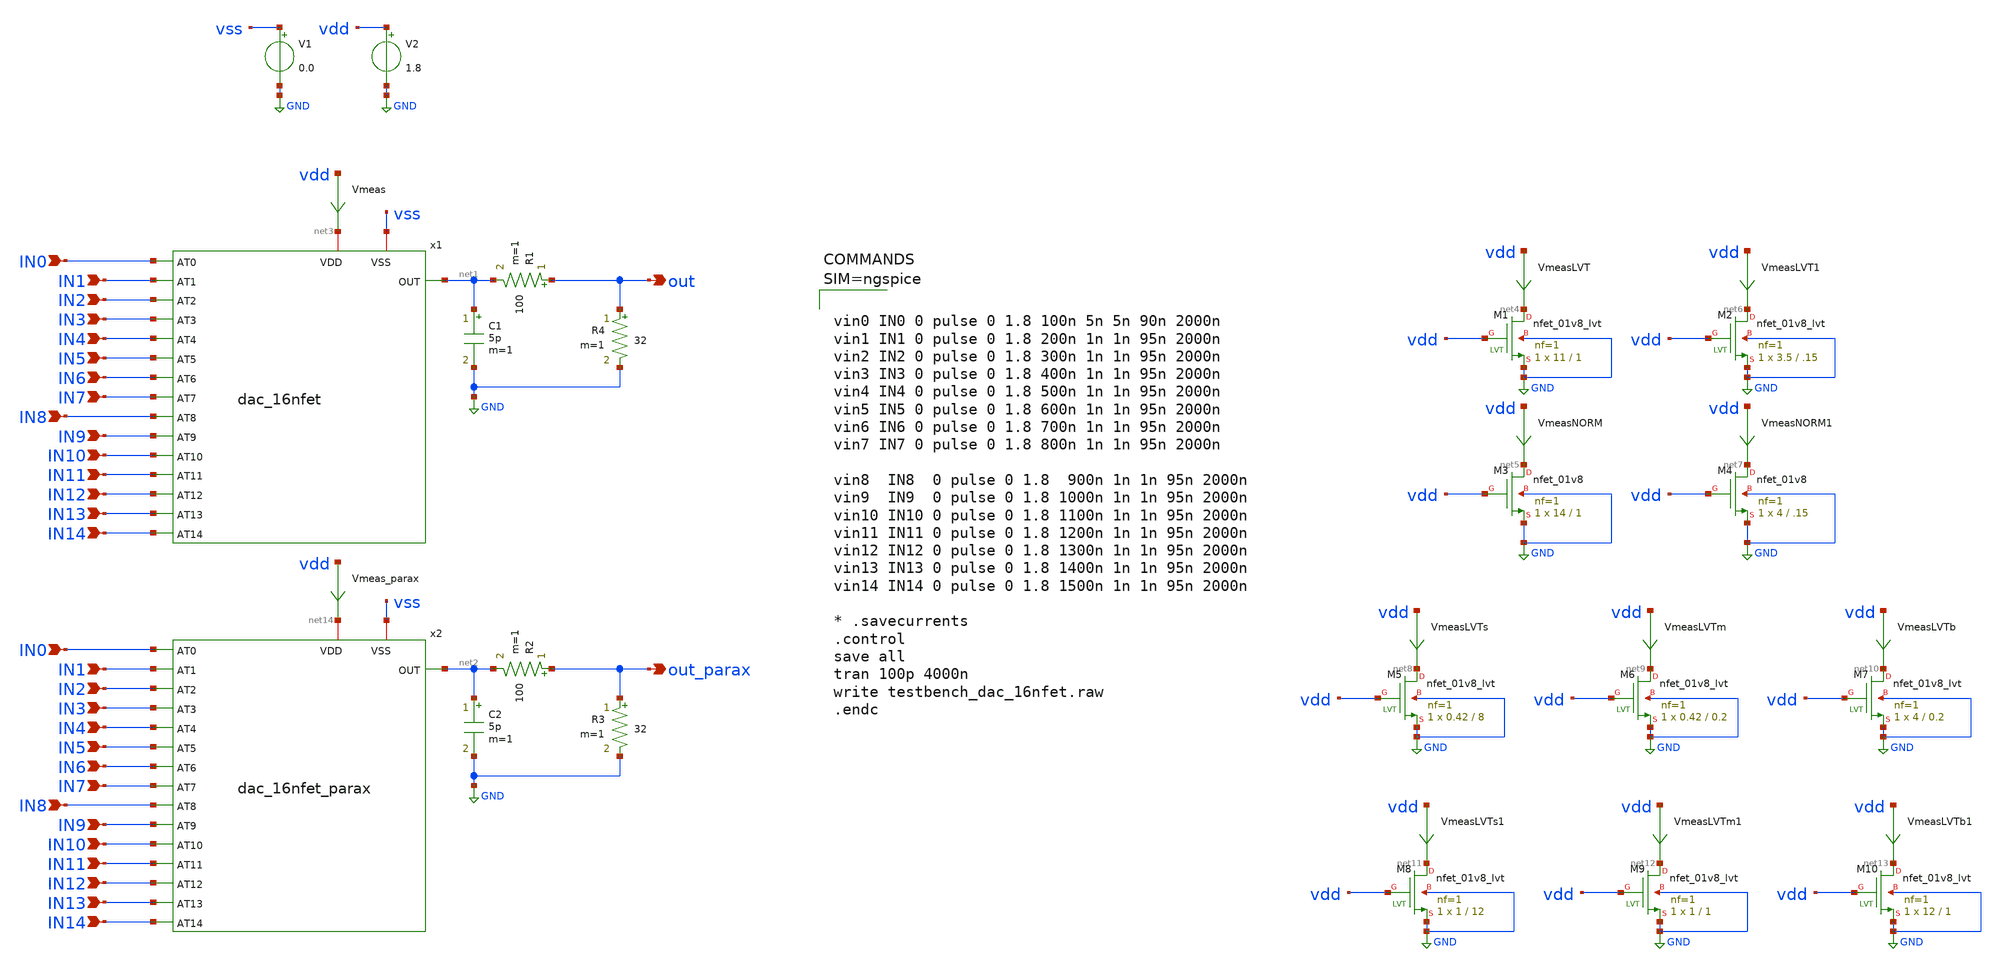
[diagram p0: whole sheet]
** sch_path: xschem/testbench_dac_16nfet.sch
**.subckt testbench_dac_16nfet IN1 out IN2 IN3 IN0 IN5 IN6 IN7 IN4 IN9 IN10 IN11 IN8 IN13 IN14 IN12
*+ IN1 out_parax IN2 IN3 IN0 IN5 IN6 IN7 IN4 IN9 IN10 IN11 IN8 IN13 IN14 IN12
*.ipin IN1
*.opin out
*.ipin IN2
*.ipin IN3
*.ipin IN0
*.ipin IN5
*.ipin IN6
*.ipin IN7
*.ipin IN4
*.ipin IN9
*.ipin IN10
*.ipin IN11
*.ipin IN8
*.ipin IN13
*.ipin IN14
*.ipin IN12
*.ipin IN1
*.opin out_parax
*.ipin IN2
*.ipin IN3
*.ipin IN0
*.ipin IN5
*.ipin IN6
*.ipin IN7
*.ipin IN4
*.ipin IN9
*.ipin IN10
*.ipin IN11
*.ipin IN8
*.ipin IN13
*.ipin IN14
*.ipin IN12
x1 net3 IN0 IN1 IN2 IN3 IN4 IN5 IN6 IN7 IN8 IN9 IN10 IN11 IN12 IN13 IN14 net1 vss dac_16nfet
V1 vss GND 0.0
V2 vdd GND 1.8
R1 out net1 100 m=1
Vmeas vdd net3 0
.save i(vmeas)
R4 out GND 32 m=1
C1 net1 GND 5p m=1
XM1 net4 vdd GND GND sky130_fd_pr__nfet_01v8_lvt L=1 W=11 nf=1 ad='int((nf+1)/2) * W/nf * 0.29' as='int((nf+2)/2) * W/nf * 0.29'
+ pd='2*int((nf+1)/2) * (W/nf + 0.29)' ps='2*int((nf+2)/2) * (W/nf + 0.29)' nrd='0.29 / W' nrs='0.29 / W'
+ sa=0 sb=0 sd=0 mult=1 m=1
VmeasLVT vdd net4 0
.save i(vmeaslvt)
XM3 net5 vdd GND GND sky130_fd_pr__nfet_01v8 L=1 W=14 nf=1 ad='int((nf+1)/2) * W/nf * 0.29' as='int((nf+2)/2) * W/nf * 0.29'
+ pd='2*int((nf+1)/2) * (W/nf + 0.29)' ps='2*int((nf+2)/2) * (W/nf + 0.29)' nrd='0.29 / W' nrs='0.29 / W'
+ sa=0 sb=0 sd=0 mult=1 m=1
VmeasNORM vdd net5 0
.save i(vmeasnorm)
XM2 net6 vdd GND GND sky130_fd_pr__nfet_01v8_lvt L=.15 W=3.5 nf=1 ad='int((nf+1)/2) * W/nf * 0.29' as='int((nf+2)/2) * W/nf * 0.29'
+ pd='2*int((nf+1)/2) * (W/nf + 0.29)' ps='2*int((nf+2)/2) * (W/nf + 0.29)' nrd='0.29 / W' nrs='0.29 / W'
+ sa=0 sb=0 sd=0 mult=1 m=1
VmeasLVT1 vdd net6 0
.save i(vmeaslvt1)
XM4 net7 vdd GND GND sky130_fd_pr__nfet_01v8 L=.15 W=4 nf=1 ad='int((nf+1)/2) * W/nf * 0.29' as='int((nf+2)/2) * W/nf * 0.29'
+ pd='2*int((nf+1)/2) * (W/nf + 0.29)' ps='2*int((nf+2)/2) * (W/nf + 0.29)' nrd='0.29 / W' nrs='0.29 / W'
+ sa=0 sb=0 sd=0 mult=1 m=1
VmeasNORM1 vdd net7 0
.save i(vmeasnorm1)
XM5 net8 vdd GND GND sky130_fd_pr__nfet_01v8_lvt L=8 W=0.42 nf=1 ad='int((nf+1)/2) * W/nf * 0.29' as='int((nf+2)/2) * W/nf * 0.29'
+ pd='2*int((nf+1)/2) * (W/nf + 0.29)' ps='2*int((nf+2)/2) * (W/nf + 0.29)' nrd='0.29 / W' nrs='0.29 / W'
+ sa=0 sb=0 sd=0 mult=1 m=1
VmeasLVTs vdd net8 0
.save i(vmeaslvts)
XM6 net9 vdd GND GND sky130_fd_pr__nfet_01v8_lvt L=0.2 W=0.42 nf=1 ad='int((nf+1)/2) * W/nf * 0.29' as='int((nf+2)/2) * W/nf * 0.29'
+ pd='2*int((nf+1)/2) * (W/nf + 0.29)' ps='2*int((nf+2)/2) * (W/nf + 0.29)' nrd='0.29 / W' nrs='0.29 / W'
+ sa=0 sb=0 sd=0 mult=1 m=1
VmeasLVTm vdd net9 0
.save i(vmeaslvtm)
XM7 net10 vdd GND GND sky130_fd_pr__nfet_01v8_lvt L=0.2 W=4 nf=1 ad='int((nf+1)/2) * W/nf * 0.29' as='int((nf+2)/2) * W/nf * 0.29'
+ pd='2*int((nf+1)/2) * (W/nf + 0.29)' ps='2*int((nf+2)/2) * (W/nf + 0.29)' nrd='0.29 / W' nrs='0.29 / W'
+ sa=0 sb=0 sd=0 mult=1 m=1
VmeasLVTb vdd net10 0
.save i(vmeaslvtb)
XM8 net11 vdd GND GND sky130_fd_pr__nfet_01v8_lvt L=12 W=1 nf=1 ad='int((nf+1)/2) * W/nf * 0.29' as='int((nf+2)/2) * W/nf * 0.29'
+ pd='2*int((nf+1)/2) * (W/nf + 0.29)' ps='2*int((nf+2)/2) * (W/nf + 0.29)' nrd='0.29 / W' nrs='0.29 / W'
+ sa=0 sb=0 sd=0 mult=1 m=1
VmeasLVTs1 vdd net11 0
.save i(vmeaslvts1)
XM9 net12 vdd GND GND sky130_fd_pr__nfet_01v8_lvt L=1 W=1 nf=1 ad='int((nf+1)/2) * W/nf * 0.29' as='int((nf+2)/2) * W/nf * 0.29'
+ pd='2*int((nf+1)/2) * (W/nf + 0.29)' ps='2*int((nf+2)/2) * (W/nf + 0.29)' nrd='0.29 / W' nrs='0.29 / W'
+ sa=0 sb=0 sd=0 mult=1 m=1
VmeasLVTm1 vdd net12 0
.save i(vmeaslvtm1)
XM10 net13 vdd GND GND sky130_fd_pr__nfet_01v8_lvt L=1 W=12 nf=1 ad='int((nf+1)/2) * W/nf * 0.29' as='int((nf+2)/2) * W/nf * 0.29'
+ pd='2*int((nf+1)/2) * (W/nf + 0.29)' ps='2*int((nf+2)/2) * (W/nf + 0.29)' nrd='0.29 / W' nrs='0.29 / W'
+ sa=0 sb=0 sd=0 mult=1 m=1
VmeasLVTb1 vdd net13 0
.save i(vmeaslvtb1)
x2 net14 IN0 IN1 IN2 IN3 IN4 IN5 IN6 IN7 IN8 IN9 IN10 IN11 IN12 IN13 IN14 net2 vss dac_16nfet_parax
R2 out_parax net2 100 m=1
Vmeas_parax vdd net14 0
.save i(vmeas_parax)
R3 out_parax GND 32 m=1
C2 net2 GND 5p m=1
**** begin user architecture code

** opencircuitdesign pdks install
.lib $::SKYWATER_MODELS/sky130.lib.spice tt





vin0 IN0 0 pulse 0 1.8 100n 5n 5n 90n 2000n
vin1 IN1 0 pulse 0 1.8 200n 1n 1n 95n 2000n
vin2 IN2 0 pulse 0 1.8 300n 1n 1n 95n 2000n
vin3 IN3 0 pulse 0 1.8 400n 1n 1n 95n 2000n
vin4 IN4 0 pulse 0 1.8 500n 1n 1n 95n 2000n
vin5 IN5 0 pulse 0 1.8 600n 1n 1n 95n 2000n
vin6 IN6 0 pulse 0 1.8 700n 1n 1n 95n 2000n
vin7 IN7 0 pulse 0 1.8 800n 1n 1n 95n 2000n

vin8  IN8  0 pulse 0 1.8  900n 1n 1n 95n 2000n
vin9  IN9  0 pulse 0 1.8 1000n 1n 1n 95n 2000n
vin10 IN10 0 pulse 0 1.8 1100n 1n 1n 95n 2000n
vin11 IN11 0 pulse 0 1.8 1200n 1n 1n 95n 2000n
vin12 IN12 0 pulse 0 1.8 1300n 1n 1n 95n 2000n
vin13 IN13 0 pulse 0 1.8 1400n 1n 1n 95n 2000n
vin14 IN14 0 pulse 0 1.8 1500n 1n 1n 95n 2000n

* .savecurrents
.control
save all
tran 100p 4000n
write testbench_dac_16nfet.raw
.endc



**** end user architecture code
**.ends

* expanding   symbol:  dac_16nfet.sym # of pins=18
** sym_path: xschem/dac_16nfet.sym
** sch_path: xschem/dac_16nfet.sch
.subckt dac_16nfet VDD AT0 AT1 AT2 AT3 AT4 AT5 AT6 AT7 AT8 AT9 AT10 AT11 AT12 AT13 AT14 OUT VSS
*.ipin AT12
*.ipin AT13
*.iopin VDD
*.iopin VSS
*.opin OUT
*.ipin AT14
*.ipin AT4
*.ipin AT5
*.ipin AT6
*.ipin AT7
*.ipin AT8
*.ipin AT9
*.ipin AT10
*.ipin AT11
*.ipin AT0
*.ipin AT1
*.ipin AT2
*.ipin AT3
XM1 VDD AT12 OUT VSS sky130_fd_pr__nfet_01v8 L=5.547 W=0.42 nf=1 ad='int((nf+1)/2) * W/nf * 0.29' as='int((nf+2)/2) * W/nf * 0.29'
+ pd='2*int((nf+1)/2) * (W/nf + 0.29)' ps='2*int((nf+2)/2) * (W/nf + 0.29)' nrd='0.29 / W' nrs='0.29 / W'
+ sa=0 sb=0 sd=0 mult=1 m=1
XM2 VDD AT13 OUT VSS sky130_fd_pr__nfet_01v8 L=7.784 W=0.42 nf=1 ad='int((nf+1)/2) * W/nf * 0.29' as='int((nf+2)/2) * W/nf * 0.29'
+ pd='2*int((nf+1)/2) * (W/nf + 0.29)' ps='2*int((nf+2)/2) * (W/nf + 0.29)' nrd='0.29 / W' nrs='0.29 / W'
+ sa=0 sb=0 sd=0 mult=1 m=1
XM3 VDD AT14 OUT VSS sky130_fd_pr__nfet_01v8 L=11.1 W=0.42 nf=1 ad='int((nf+1)/2) * W/nf * 0.29' as='int((nf+2)/2) * W/nf * 0.29'
+ pd='2*int((nf+1)/2) * (W/nf + 0.29)' ps='2*int((nf+2)/2) * (W/nf + 0.29)' nrd='0.29 / W' nrs='0.29 / W'
+ sa=0 sb=0 sd=0 mult=1 m=1
XM5 VDD AT8 OUT VSS sky130_fd_pr__nfet_01v8 L=1.386 W=0.42 nf=1 ad='int((nf+1)/2) * W/nf * 0.29' as='int((nf+2)/2) * W/nf * 0.29'
+ pd='2*int((nf+1)/2) * (W/nf + 0.29)' ps='2*int((nf+2)/2) * (W/nf + 0.29)' nrd='0.29 / W' nrs='0.29 / W'
+ sa=0 sb=0 sd=0 mult=1 m=1
XM6 VDD AT9 OUT VSS sky130_fd_pr__nfet_01v8 L=1.96 W=0.42 nf=1 ad='int((nf+1)/2) * W/nf * 0.29' as='int((nf+2)/2) * W/nf * 0.29'
+ pd='2*int((nf+1)/2) * (W/nf + 0.29)' ps='2*int((nf+2)/2) * (W/nf + 0.29)' nrd='0.29 / W' nrs='0.29 / W'
+ sa=0 sb=0 sd=0 mult=1 m=1
XM7 VDD AT10 OUT VSS sky130_fd_pr__nfet_01v8 L=2.773 W=0.42 nf=1 ad='int((nf+1)/2) * W/nf * 0.29' as='int((nf+2)/2) * W/nf * 0.29'
+ pd='2*int((nf+1)/2) * (W/nf + 0.29)' ps='2*int((nf+2)/2) * (W/nf + 0.29)' nrd='0.29 / W' nrs='0.29 / W'
+ sa=0 sb=0 sd=0 mult=1 m=1
XM8 VDD AT11 OUT VSS sky130_fd_pr__nfet_01v8 L=3.922 W=0.42 nf=1 ad='int((nf+1)/2) * W/nf * 0.29' as='int((nf+2)/2) * W/nf * 0.29'
+ pd='2*int((nf+1)/2) * (W/nf + 0.29)' ps='2*int((nf+2)/2) * (W/nf + 0.29)' nrd='0.29 / W' nrs='0.29 / W'
+ sa=0 sb=0 sd=0 mult=1 m=1
XM9 VDD AT4 OUT VSS sky130_fd_pr__nfet_01v8 L=0.98 W=1.188 nf=1 ad='int((nf+1)/2) * W/nf * 0.29' as='int((nf+2)/2) * W/nf * 0.29'
+ pd='2*int((nf+1)/2) * (W/nf + 0.29)' ps='2*int((nf+2)/2) * (W/nf + 0.29)' nrd='0.29 / W' nrs='0.29 / W'
+ sa=0 sb=0 sd=0 mult=1 m=1
XM10 VDD AT5 OUT VSS sky130_fd_pr__nfet_01v8 L=0.98 W=0.84 nf=1 ad='int((nf+1)/2) * W/nf * 0.29' as='int((nf+2)/2) * W/nf * 0.29'
+ pd='2*int((nf+1)/2) * (W/nf + 0.29)' ps='2*int((nf+2)/2) * (W/nf + 0.29)' nrd='0.29 / W' nrs='0.29 / W'
+ sa=0 sb=0 sd=0 mult=1 m=1
XM11 VDD AT6 OUT VSS sky130_fd_pr__nfet_01v8 L=0.98 W=0.6 nf=1 ad='int((nf+1)/2) * W/nf * 0.29' as='int((nf+2)/2) * W/nf * 0.29'
+ pd='2*int((nf+1)/2) * (W/nf + 0.29)' ps='2*int((nf+2)/2) * (W/nf + 0.29)' nrd='0.29 / W' nrs='0.29 / W'
+ sa=0 sb=0 sd=0 mult=1 m=1
XM12 VDD AT7 OUT VSS sky130_fd_pr__nfet_01v8 L=0.98 W=0.42 nf=1 ad='int((nf+1)/2) * W/nf * 0.29' as='int((nf+2)/2) * W/nf * 0.29'
+ pd='2*int((nf+1)/2) * (W/nf + 0.29)' ps='2*int((nf+2)/2) * (W/nf + 0.29)' nrd='0.29 / W' nrs='0.29 / W'
+ sa=0 sb=0 sd=0 mult=1 m=1
XM13 VDD AT0 OUT VSS sky130_fd_pr__nfet_01v8 L=0.98 W=4.756 nf=1 ad='int((nf+1)/2) * W/nf * 0.29' as='int((nf+2)/2) * W/nf * 0.29'
+ pd='2*int((nf+1)/2) * (W/nf + 0.29)' ps='2*int((nf+2)/2) * (W/nf + 0.29)' nrd='0.29 / W' nrs='0.29 / W'
+ sa=0 sb=0 sd=0 mult=1 m=1
XM14 VDD AT1 OUT VSS sky130_fd_pr__nfet_01v8 L=0.98 W=3.363 nf=1 ad='int((nf+1)/2) * W/nf * 0.29' as='int((nf+2)/2) * W/nf * 0.29'
+ pd='2*int((nf+1)/2) * (W/nf + 0.29)' ps='2*int((nf+2)/2) * (W/nf + 0.29)' nrd='0.29 / W' nrs='0.29 / W'
+ sa=0 sb=0 sd=0 mult=1 m=1
XM15 VDD AT2 OUT VSS sky130_fd_pr__nfet_01v8 L=0.98 W=2.377 nf=1 ad='int((nf+1)/2) * W/nf * 0.29' as='int((nf+2)/2) * W/nf * 0.29'
+ pd='2*int((nf+1)/2) * (W/nf + 0.29)' ps='2*int((nf+2)/2) * (W/nf + 0.29)' nrd='0.29 / W' nrs='0.29 / W'
+ sa=0 sb=0 sd=0 mult=1 m=1
XM16 VDD AT3 OUT VSS sky130_fd_pr__nfet_01v8 L=0.98 W=1.681 nf=1 ad='int((nf+1)/2) * W/nf * 0.29' as='int((nf+2)/2) * W/nf * 0.29'
+ pd='2*int((nf+1)/2) * (W/nf + 0.29)' ps='2*int((nf+2)/2) * (W/nf + 0.29)' nrd='0.29 / W' nrs='0.29 / W'
+ sa=0 sb=0 sd=0 mult=1 m=1
.ends


* expanding   symbol:  dac_16nfet_parax.sym # of pins=18
** sym_path: xschem/dac_16nfet.sym
.include [file normalize ../mag/dac_16nfet.sim.spice]
.GLOBAL GND
.end
